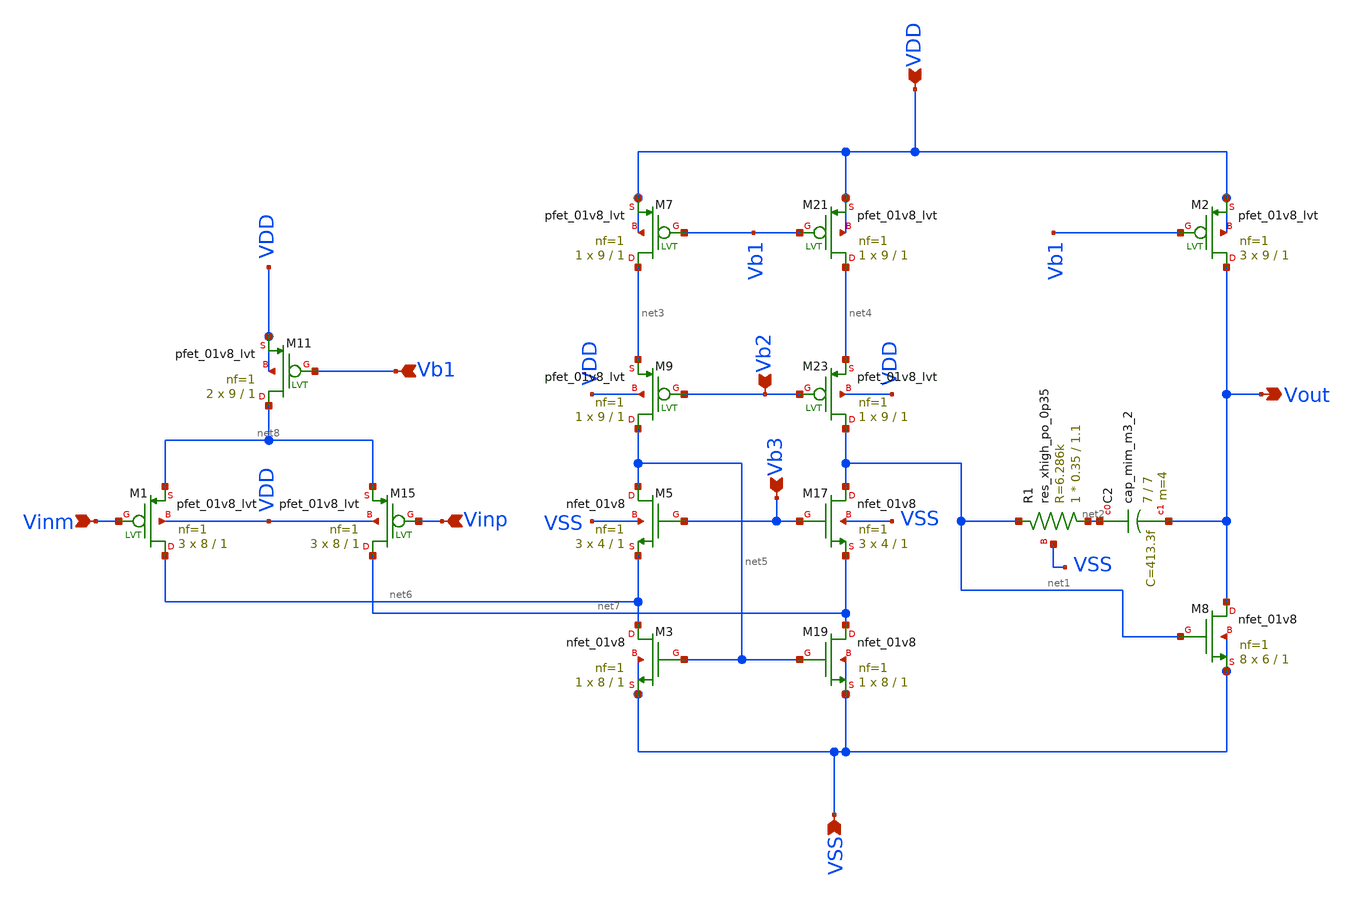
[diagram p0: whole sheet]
** sch_path: xschem/2stageOpamp.sch
**.subckt 2stageOpamp Vinm Vinp Vout VSS VDD Vb1 Vb2 Vb3
*.ipin Vinm
*.ipin Vinp
*.opin Vout
*.ipin VSS
*.ipin VDD
*.ipin Vb1
*.ipin Vb2
*.ipin Vb3
XM8 Vout net1 VSS VSS sky130_fd_pr__nfet_01v8 L=1 W=6 nf=1 ad='int((nf+1)/2) * W/nf * 0.29' as='int((nf+2)/2) * W/nf * 0.29'
+ pd='2*int((nf+1)/2) * (W/nf + 0.29)' ps='2*int((nf+2)/2) * (W/nf + 0.29)' nrd='0.29 / W' nrs='0.29 / W'
+ sa=0 sb=0 sd=0 mult=8 m=8
XM2 Vout Vb1 VDD VDD sky130_fd_pr__pfet_01v8_lvt L=1 W=9 nf=1 ad='int((nf+1)/2) * W/nf * 0.29' as='int((nf+2)/2) * W/nf * 0.29'
+ pd='2*int((nf+1)/2) * (W/nf + 0.29)' ps='2*int((nf+2)/2) * (W/nf + 0.29)' nrd='0.29 / W' nrs='0.29 / W'
+ sa=0 sb=0 sd=0 mult=3 m=3
XC2 net2 Vout sky130_fd_pr__cap_mim_m3_2 W=7 L=7 MF=4 m=4
XM5 net5 Vb3 net6 VSS sky130_fd_pr__nfet_01v8 L=1 W=4 nf=1 ad='int((nf+1)/2) * W/nf * 0.29' as='int((nf+2)/2) * W/nf * 0.29'
+ pd='2*int((nf+1)/2) * (W/nf + 0.29)' ps='2*int((nf+2)/2) * (W/nf + 0.29)' nrd='0.29 / W' nrs='0.29 / W'
+ sa=0 sb=0 sd=0 mult=3 m=3
XM17 net1 Vb3 net7 VSS sky130_fd_pr__nfet_01v8 L=1 W=4 nf=1 ad='int((nf+1)/2) * W/nf * 0.29' as='int((nf+2)/2) * W/nf * 0.29'
+ pd='2*int((nf+1)/2) * (W/nf + 0.29)' ps='2*int((nf+2)/2) * (W/nf + 0.29)' nrd='0.29 / W' nrs='0.29 / W'
+ sa=0 sb=0 sd=0 mult=3 m=3
XM3 net6 net5 VSS VSS sky130_fd_pr__nfet_01v8 L=1 W=8 nf=1 ad='int((nf+1)/2) * W/nf * 0.29' as='int((nf+2)/2) * W/nf * 0.29'
+ pd='2*int((nf+1)/2) * (W/nf + 0.29)' ps='2*int((nf+2)/2) * (W/nf + 0.29)' nrd='0.29 / W' nrs='0.29 / W'
+ sa=0 sb=0 sd=0 mult=1 m=1
XM19 net7 net5 VSS VSS sky130_fd_pr__nfet_01v8 L=1 W=8 nf=1 ad='int((nf+1)/2) * W/nf * 0.29' as='int((nf+2)/2) * W/nf * 0.29'
+ pd='2*int((nf+1)/2) * (W/nf + 0.29)' ps='2*int((nf+2)/2) * (W/nf + 0.29)' nrd='0.29 / W' nrs='0.29 / W'
+ sa=0 sb=0 sd=0 mult=1 m=1
XM11 net8 Vb1 VDD VDD sky130_fd_pr__pfet_01v8_lvt L=1 W=9 nf=1 ad='int((nf+1)/2) * W/nf * 0.29' as='int((nf+2)/2) * W/nf * 0.29'
+ pd='2*int((nf+1)/2) * (W/nf + 0.29)' ps='2*int((nf+2)/2) * (W/nf + 0.29)' nrd='0.29 / W' nrs='0.29 / W'
+ sa=0 sb=0 sd=0 mult=2 m=2
XM1 net6 Vinm net8 VDD sky130_fd_pr__pfet_01v8_lvt L=1 W=8 nf=1 ad='int((nf+1)/2) * W/nf * 0.29' as='int((nf+2)/2) * W/nf * 0.29'
+ pd='2*int((nf+1)/2) * (W/nf + 0.29)' ps='2*int((nf+2)/2) * (W/nf + 0.29)' nrd='0.29 / W' nrs='0.29 / W'
+ sa=0 sb=0 sd=0 mult=3 m=3
XM15 net7 Vinp net8 VDD sky130_fd_pr__pfet_01v8_lvt L=1 W=8 nf=1 ad='int((nf+1)/2) * W/nf * 0.29' as='int((nf+2)/2) * W/nf * 0.29'
+ pd='2*int((nf+1)/2) * (W/nf + 0.29)' ps='2*int((nf+2)/2) * (W/nf + 0.29)' nrd='0.29 / W' nrs='0.29 / W'
+ sa=0 sb=0 sd=0 mult=3 m=3
XM7 net3 Vb1 VDD VDD sky130_fd_pr__pfet_01v8_lvt L=1 W=9 nf=1 ad='int((nf+1)/2) * W/nf * 0.29' as='int((nf+2)/2) * W/nf * 0.29'
+ pd='2*int((nf+1)/2) * (W/nf + 0.29)' ps='2*int((nf+2)/2) * (W/nf + 0.29)' nrd='0.29 / W' nrs='0.29 / W'
+ sa=0 sb=0 sd=0 mult=1 m=1
XM21 net4 Vb1 VDD VDD sky130_fd_pr__pfet_01v8_lvt L=1 W=9 nf=1 ad='int((nf+1)/2) * W/nf * 0.29' as='int((nf+2)/2) * W/nf * 0.29'
+ pd='2*int((nf+1)/2) * (W/nf + 0.29)' ps='2*int((nf+2)/2) * (W/nf + 0.29)' nrd='0.29 / W' nrs='0.29 / W'
+ sa=0 sb=0 sd=0 mult=1 m=1
XM9 net5 Vb2 net3 VDD sky130_fd_pr__pfet_01v8_lvt L=1 W=9 nf=1 ad='int((nf+1)/2) * W/nf * 0.29' as='int((nf+2)/2) * W/nf * 0.29'
+ pd='2*int((nf+1)/2) * (W/nf + 0.29)' ps='2*int((nf+2)/2) * (W/nf + 0.29)' nrd='0.29 / W' nrs='0.29 / W'
+ sa=0 sb=0 sd=0 mult=1 m=1
XM23 net1 Vb2 net4 VDD sky130_fd_pr__pfet_01v8_lvt L=1 W=9 nf=1 ad='int((nf+1)/2) * W/nf * 0.29' as='int((nf+2)/2) * W/nf * 0.29'
+ pd='2*int((nf+1)/2) * (W/nf + 0.29)' ps='2*int((nf+2)/2) * (W/nf + 0.29)' nrd='0.29 / W' nrs='0.29 / W'
+ sa=0 sb=0 sd=0 mult=1 m=1
XR1 net2 net1 VSS sky130_fd_pr__res_xhigh_po_0p35 L=1.1 mult=1 m=1
**.ends
.end
